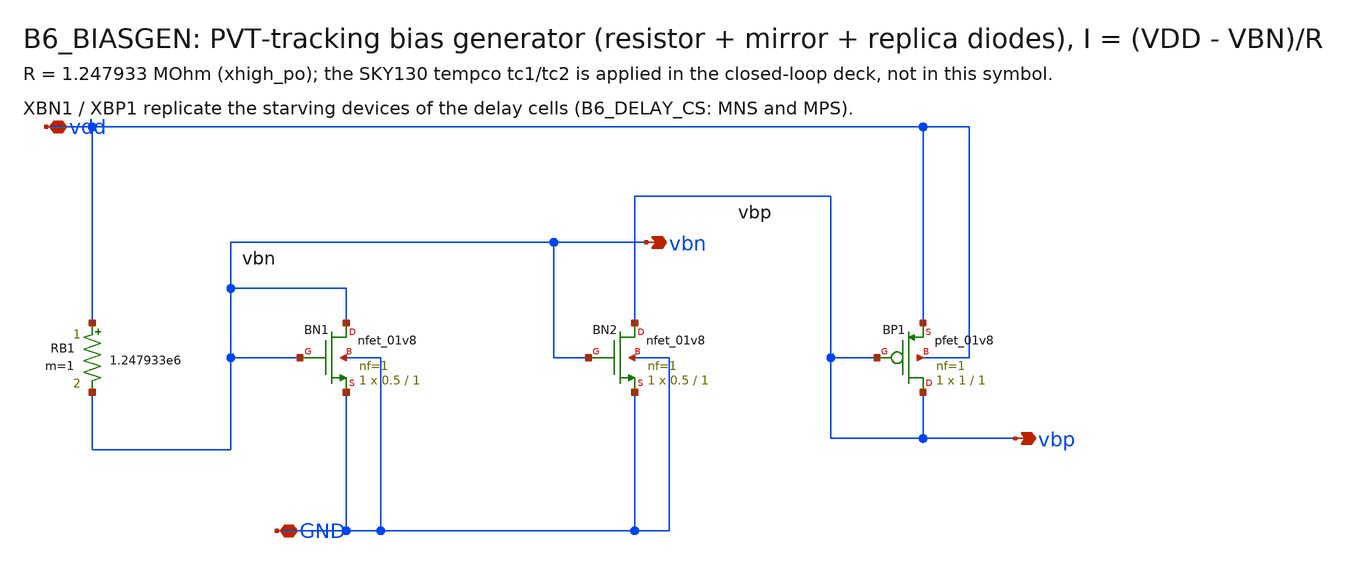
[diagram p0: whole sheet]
** sch_path: blocks/06_Clock_gen/xschem/B6_BIASGEN.sch
**.subckt B6_BIASGEN vdd GND vbn vbp
*.iopin vdd
*.iopin GND
*.opin vbn
*.opin vbp
RB1 vdd vbn 1.247933e6 m=1
XBN1 vbn vbn GND GND sky130_fd_pr__nfet_01v8 L=1 W=0.5 nf=1 ad='int((1 + 1)/2) * 0.5 / 1 * 0.29' as='int((1 + 2)/2) * 0.5 / 1 * 0.29'
+ pd='2*int((1 + 1)/2) * (0.5 / 1 + 0.29)' ps='2*int((1 + 2)/2) * (0.5 / 1 + 0.29)' nrd='0.29 / 0.5 ' nrs='0.29 / 0.5 '
+ sa=0 sb=0 sd=0 mult=1 m=1
XBN2 vbp vbn GND GND sky130_fd_pr__nfet_01v8 L=1 W=0.5 nf=1 ad='int((1 + 1)/2) * 0.5 / 1 * 0.29' as='int((1 + 2)/2) * 0.5 / 1 * 0.29'
+ pd='2*int((1 + 1)/2) * (0.5 / 1 + 0.29)' ps='2*int((1 + 2)/2) * (0.5 / 1 + 0.29)' nrd='0.29 / 0.5 ' nrs='0.29 / 0.5 '
+ sa=0 sb=0 sd=0 mult=1 m=1
XBP1 vbp vbp vdd vdd sky130_fd_pr__pfet_01v8 L=1 W=1 nf=1 ad='int((1 + 1)/2) * 1 / 1 * 0.29' as='int((1 + 2)/2) * 1 / 1 * 0.29'
+ pd='2*int((1 + 1)/2) * (1 / 1 + 0.29)' ps='2*int((1 + 2)/2) * (1 / 1 + 0.29)' nrd='0.29 / 1 ' nrs='0.29 / 1 '
+ sa=0 sb=0 sd=0 mult=1 m=1
**.ends
.end
